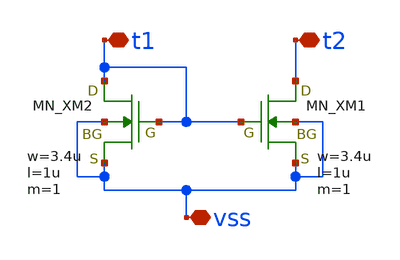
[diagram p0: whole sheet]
** sch_path: member_project/JJY_Receiver/Masahiro/jjy_recv/check_fet/check_lvs.sch
**.subckt check_lvs t1 t2 vss
*.iopin t1
*.iopin t2
*.iopin vss
XXM1 t2 t1 vss vss NMOS w=3.4u l=1u nrd=0 nrs=0 m=1
XXM2 t1 t1 vss vss NMOS w=3.4u l=1u nrd=0 nrs=0 m=1
**.ends
.end
